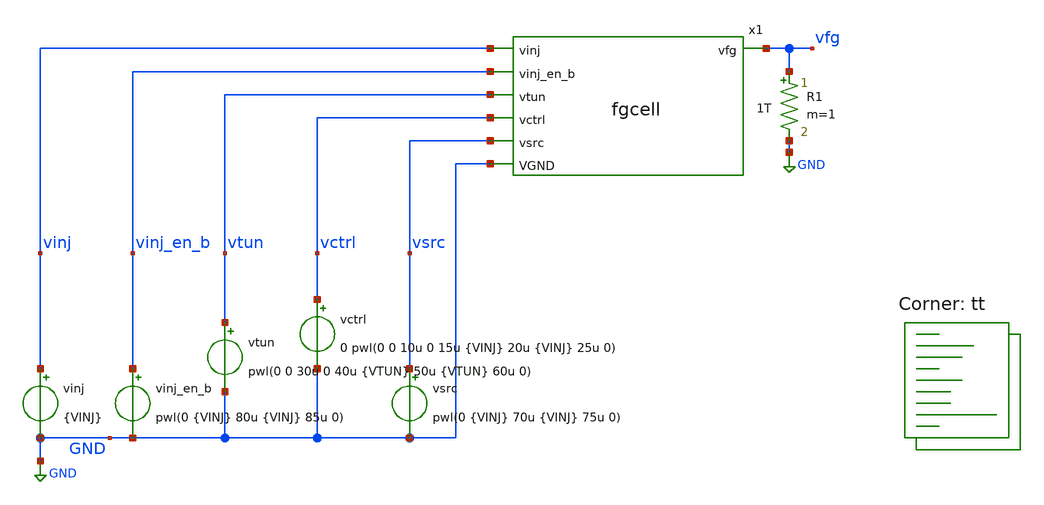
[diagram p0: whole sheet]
** sch_path: xschem/test-fgcell.sch
**.subckt test-fgcell
x1 vinj vinj_en_b vfg vtun vctrl vsrc GND fgcell
vinj_en_b vinj_en_b GND pwl(0 {VINJ} 80u {VINJ} 85u 0)
vctrl vctrl GND 0 pwl(0 0 10u 0 15u {VINJ} 20u {VINJ} 25u 0)
vsrc vsrc GND pwl(0 {VINJ} 70u {VINJ} 75u 0)
vtun vtun GND pwl(0 0 30u 0 40u {VTUN} 50u {VTUN} 60u 0)
vinj vinj GND {VINJ}
R1 vfg GND 1T m=1
**** begin user architecture code
.lib $::SKYWATER_MODELS/sky130.lib.spice tt



.options reltol=0.0001 abstol=10e-15 chgtol=1e-15
* .include fgcell.spice
.param VTUN=12
.param VINJ=6
.param VDD=1.8
.param VSS=0
.option savecurrents
.ic v(vinj)=6 v(vinj_en_b)=6 v(vtun)=0 v(vsrc)=6 v(vfg)=0 v(x1.net1)=6
.control
  save all
  *op
  *remzerovec
  *write test-fgcell.raw
  *set appendwrite
  tran 10n 120u uic
  remzerovec
  write test-fgcell.raw
.endc



**** end user architecture code
**.ends

* expanding   symbol:  fgcell.sym # of pins=7
** sym_path: xschem/fgcell.sym
** sch_path: xschem/fgcell.sch
.subckt fgcell vinj vinj_en_b vfg vtun vctrl vsrc VGND
*.ipin vinj
*.ipin vinj_en_b
*.ipin vtun
*.ipin vctrl
*.ipin vsrc
*.ipin VGND
*.opin vfg
XM1 vsrc vfg net1 vinj sky130_fd_pr__pfet_g5v0d10v5 L=0.5 W=1 nf=1 ad='int((nf+1)/2) * W/nf * 0.29' as='int((nf+2)/2) * W/nf * 0.29'
+ pd='2*int((nf+1)/2) * (W/nf + 0.29)' ps='2*int((nf+2)/2) * (W/nf + 0.29)' nrd='0.29 / W' nrs='0.29 / W'
+ sa=0 sb=0 sd=0 mult=1 m=1
XM2 net1 vinj_en_b vinj vinj sky130_fd_pr__pfet_g5v0d10v5 L=0.5 W=1 nf=1 ad='int((nf+1)/2) * W/nf * 0.29'
+ as='int((nf+2)/2) * W/nf * 0.29' pd='2*int((nf+1)/2) * (W/nf + 0.29)' ps='2*int((nf+2)/2) * (W/nf + 0.29)'
+ nrd='0.29 / W' nrs='0.29 / W' sa=0 sb=0 sd=0 mult=1 m=1
XC1 vfg vtun VGND sky130_fd_pr__cap_var_hvt W=1 L=0.5 VM=1 m=1
XM3 vctrl vfg vctrl vctrl sky130_fd_pr__pfet_g5v0d10v5 L=0.5 W=1 nf=1 ad='int((nf+1)/2) * W/nf * 0.29'
+ as='int((nf+2)/2) * W/nf * 0.29' pd='2*int((nf+1)/2) * (W/nf + 0.29)' ps='2*int((nf+2)/2) * (W/nf + 0.29)'
+ nrd='0.29 / W' nrs='0.29 / W' sa=0 sb=0 sd=0 mult=1 m=1
.ends

.GLOBAL GND
.end
